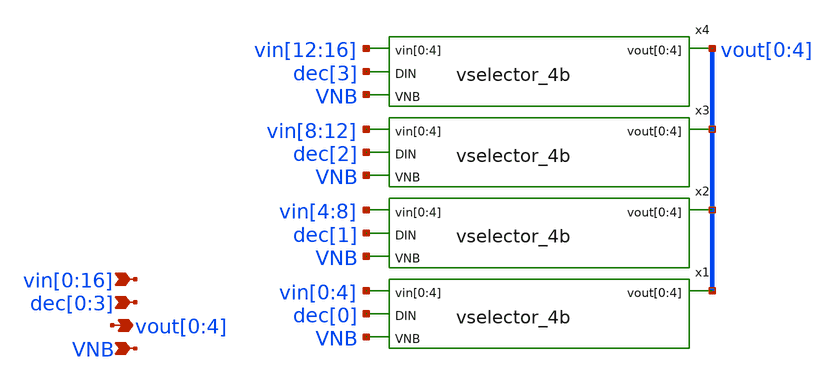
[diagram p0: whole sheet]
** sch_path: xschem/vselector_6b_2v_stage_2.sch
**.subckt vselector_6b_2v_stage_2
*+ vin[0],vin[1],vin[2],vin[3],vin[4],vin[5],vin[6],vin[7],vin[8],vin[9],vin[10],vin[11],vin[12],vin[13],vin[14],vin[15],vin[16] vout[0],vout[1],vout[2],vout[3],vout[4] VNB dec[0],dec[1],dec[2],dec[3]
*.ipin
*+ vin[0],vin[1],vin[2],vin[3],vin[4],vin[5],vin[6],vin[7],vin[8],vin[9],vin[10],vin[11],vin[12],vin[13],vin[14],vin[15],vin[16]
*.opin vout[0],vout[1],vout[2],vout[3],vout[4]
*.ipin VNB
*.ipin dec[0],dec[1],dec[2],dec[3]
x1 vin[0] vin[1] vin[2] vin[3] vin[4] dec[0] vout[0] vout[1] vout[2] vout[3] vout[4] VNB
+ vselector_4b
x2 vin[4] vin[5] vin[6] vin[7] vin[8] dec[1] vout[0] vout[1] vout[2] vout[3] vout[4] VNB
+ vselector_4b
x3 vin[8] vin[9] vin[10] vin[11] vin[12] dec[2] vout[0] vout[1] vout[2] vout[3] vout[4] VNB
+ vselector_4b
x4 vin[12] vin[13] vin[14] vin[15] vin[16] dec[3] vout[0] vout[1] vout[2] vout[3] vout[4] VNB
+ vselector_4b
**.ends

* expanding   symbol:  vselector_4b.sym # of pins=4
** sym_path: xschem/vselector_4b.sym
** sch_path: xschem/vselector_4b.sch
.subckt vselector_4b vin[0] vin[1] vin[2] vin[3] vin[4] DIN vout[0] vout[1] vout[2] vout[3] vout[4]
+ VNB
*.ipin vin[0],vin[1],vin[2],vin[3],vin[4]
*.opin vout[0],vout[1],vout[2],vout[3],vout[4]
*.ipin VNB
*.ipin DIN
XM1 vout[0] DIN vin[0] VNB sky130_fd_pr__nfet_g5v0d10v5 L=l W=wn nf=1 ad='int((nf+1)/2) * W/nf * 0.29'
+ as='int((nf+2)/2) * W/nf * 0.29' pd='2*int((nf+1)/2) * (W/nf + 0.29)' ps='2*int((nf+2)/2) * (W/nf + 0.29)'
+ nrd='0.29 / W' nrs='0.29 / W' sa=0 sb=0 sd=0 mult=1 m=1
XM2 vout[1] DIN vin[1] VNB sky130_fd_pr__nfet_g5v0d10v5 L=l W=wn nf=1 ad='int((nf+1)/2) * W/nf * 0.29'
+ as='int((nf+2)/2) * W/nf * 0.29' pd='2*int((nf+1)/2) * (W/nf + 0.29)' ps='2*int((nf+2)/2) * (W/nf + 0.29)'
+ nrd='0.29 / W' nrs='0.29 / W' sa=0 sb=0 sd=0 mult=1 m=1
XM3 vout[2] DIN vin[2] VNB sky130_fd_pr__nfet_g5v0d10v5 L=l W=wn nf=1 ad='int((nf+1)/2) * W/nf * 0.29'
+ as='int((nf+2)/2) * W/nf * 0.29' pd='2*int((nf+1)/2) * (W/nf + 0.29)' ps='2*int((nf+2)/2) * (W/nf + 0.29)'
+ nrd='0.29 / W' nrs='0.29 / W' sa=0 sb=0 sd=0 mult=1 m=1
XM4 vout[3] DIN vin[3] VNB sky130_fd_pr__nfet_g5v0d10v5 L=l W=wn nf=1 ad='int((nf+1)/2) * W/nf * 0.29'
+ as='int((nf+2)/2) * W/nf * 0.29' pd='2*int((nf+1)/2) * (W/nf + 0.29)' ps='2*int((nf+2)/2) * (W/nf + 0.29)'
+ nrd='0.29 / W' nrs='0.29 / W' sa=0 sb=0 sd=0 mult=1 m=1
XM5 vout[4] DIN vin[4] VNB sky130_fd_pr__nfet_g5v0d10v5 L=l W=wn nf=1 ad='int((nf+1)/2) * W/nf * 0.29'
+ as='int((nf+2)/2) * W/nf * 0.29' pd='2*int((nf+1)/2) * (W/nf + 0.29)' ps='2*int((nf+2)/2) * (W/nf + 0.29)'
+ nrd='0.29 / W' nrs='0.29 / W' sa=0 sb=0 sd=0 mult=1 m=1
.ends

.end
